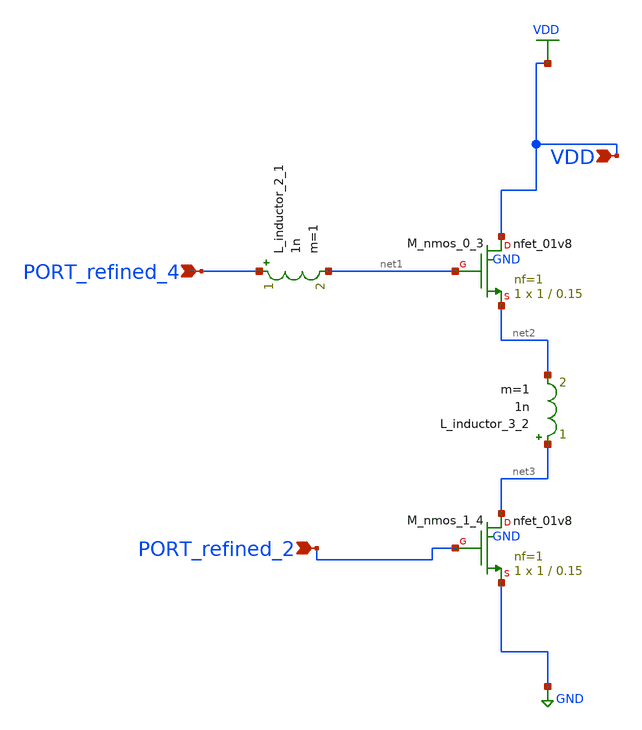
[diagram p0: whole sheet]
** sch_path: schematics/no_doi_74_001.sch
**.subckt no_doi_74_001 VDD PORT_refined_2 PORT_refined_4
*.ipin VDD
*.ipin PORT_refined_2
*.ipin PORT_refined_4
L_inductor_2_1 PORT_refined_4 net1 1n m=1
L_inductor_3_2 net3 net2 1n m=1
XM_nmos_0_3 VDD net1 net2 GND sky130_fd_pr__nfet_01v8 L=0.15 W=1 nf=1 ad='int((1 + 1)/2) * 1 / 1 * 0.29'
+ as='int((1 + 2)/2) * 1 / 1 * 0.29' pd='2*int((1 + 1)/2) * (1 / 1 + 0.29)' ps='2*int((1 + 2)/2) * (1 / 1 + 0.29)'
+ nrd='0.29 / 1 ' nrs='0.29 / 1 ' sa=0 sb=0 sd=0 mult=1 m=1
XM_nmos_1_4 net3 PORT_refined_2 GND GND sky130_fd_pr__nfet_01v8 L=0.15 W=1 nf=1 ad='int((1 + 1)/2) * 1 / 1 * 0.29'
+ as='int((1 + 2)/2) * 1 / 1 * 0.29' pd='2*int((1 + 1)/2) * (1 / 1 + 0.29)' ps='2*int((1 + 2)/2) * (1 / 1 + 0.29)'
+ nrd='0.29 / 1 ' nrs='0.29 / 1 ' sa=0 sb=0 sd=0 mult=1 m=1
**.ends
.GLOBAL GND
.GLOBAL VDD
.end
